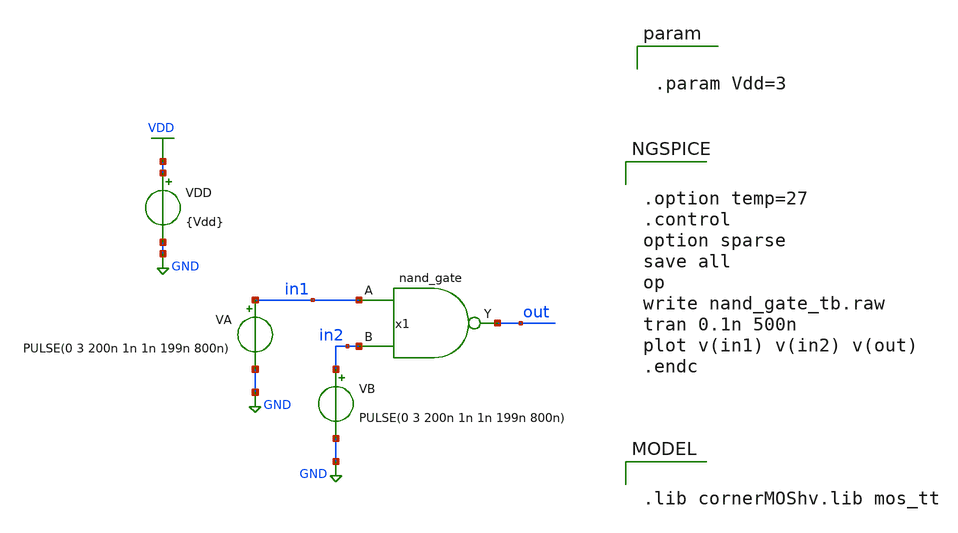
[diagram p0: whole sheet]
** sch_path: 3_real_circuits/nand_gate_tb.sch
**.subckt nand_gate_tb
x1 in1 in2 out nand_gate
VA in1 GND PULSE(0 3 200n 1n 1n 199n 800n)
VB in2 GND PULSE(0 3 200n 1n 1n 199n 800n)
VDD VDD GND {Vdd}
**** begin user architecture code


.param Vdd=3




.option temp=27
.control
option sparse
save all
op
write nand_gate_tb.raw
tran 0.1n 500n
plot v(in1) v(in2) v(out)
.endc



.lib cornerMOShv.lib mos_tt

**** end user architecture code
**.ends

* expanding   symbol:  nand_gate.sym # of pins=3
** sym_path: 3_real_circuits/nand_gate.sym
** sch_path: 3_real_circuits/nand_gate.sch
.subckt nand_gate A B Y
*.ipin A
*.ipin B
*.opin Y
XM1 Y B VDD VDD sg13_hv_pmos w=0.3u l=0.4u ng=1 m=1 mm_ok=1
XM2 Y A VDD VDD sg13_hv_pmos w=0.3u l=0.4u ng=1 m=1 mm_ok=1
XM3 Y A net1 GND sg13_hv_nmos w=0.3u l=0.45u ng=1 m=1 mm_ok=1
XM4 net1 B GND GND sg13_hv_nmos w=0.3u l=0.45u ng=1 m=1 mm_ok=1
.ends

.GLOBAL GND
.GLOBAL VDD
.end
